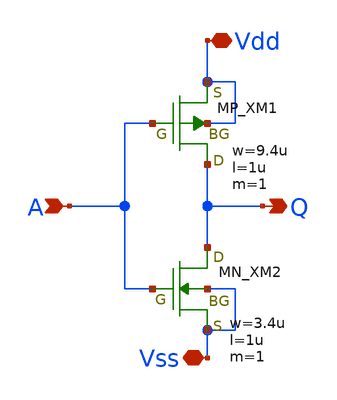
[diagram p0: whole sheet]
** sch_path: inverter/inverter_Seigo_Mitarai.sch
**.subckt inverter_Seigo_Mitarai A Q Vdd Vss
*.ipin A
*.opin Q
*.iopin Vdd
*.iopin Vss
XXM1 Q A Vdd Vdd PMOS w=9.4u l=1u nrd=0 nrs=0 m=1
XXM2 Q A Vss Vss NMOS w=3.4u l=1u nrd=0 nrs=0 m=1
**.ends
.end
